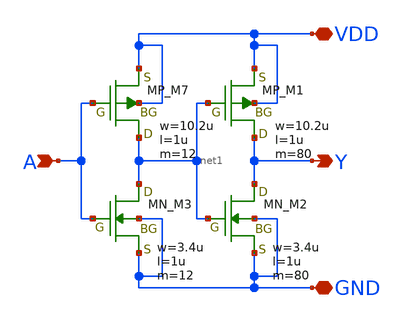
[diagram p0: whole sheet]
** sch_path: libs.tech/xschem/TR-1um_5_stdcell/CLKBUF_X16.sch
**.subckt CLKBUF_X16 A Y VDD GND
*.ipin A
*.opin Y
*.iopin VDD
*.iopin GND
XM7 net1 A VDD VDD PMOS w=10.2u l=1u nrd=0 nrs=0 m=12
XM1 Y net1 VDD VDD PMOS w=10.2u l=1u nrd=0 nrs=0 m=80
XM3 net1 A GND GND NMOS w=3.4u l=1u nrd=0 nrs=0 m=12
XM2 Y net1 GND GND NMOS w=3.4u l=1u nrd=0 nrs=0 m=80
**.ends
.end
